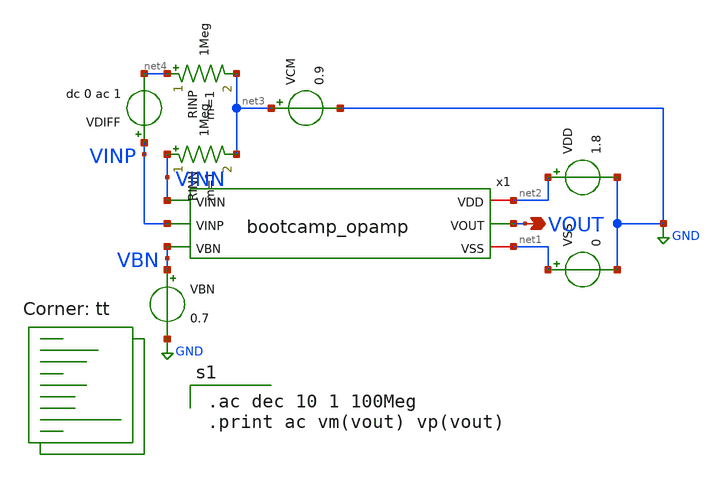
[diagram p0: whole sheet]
** sch_path: analog/bootcamp_opamp/schematics/tb_ac_analysis.sch
**.subckt tb_ac_analysis VOUT
*.opin VOUT
x1 VINN net2 net1 VINP VOUT VBN bootcamp_opamp
VDD net2 GND 1.8
VSS net1 GND 0
VCM net3 GND 0.9
RINP net4 net3 1Meg m=1
RINN VINN net3 1Meg m=1
VDIFF VINP net4 dc 0 ac 1
VBN VBN GND 0.7
**** begin user architecture code
.lib $::SKYWATER_MODELS/sky130.lib.spice tt

.ac dec 10 1 100Meg
.print ac vm(vout) vp(vout)

**** end user architecture code
**.ends
.GLOBAL GND
.end
